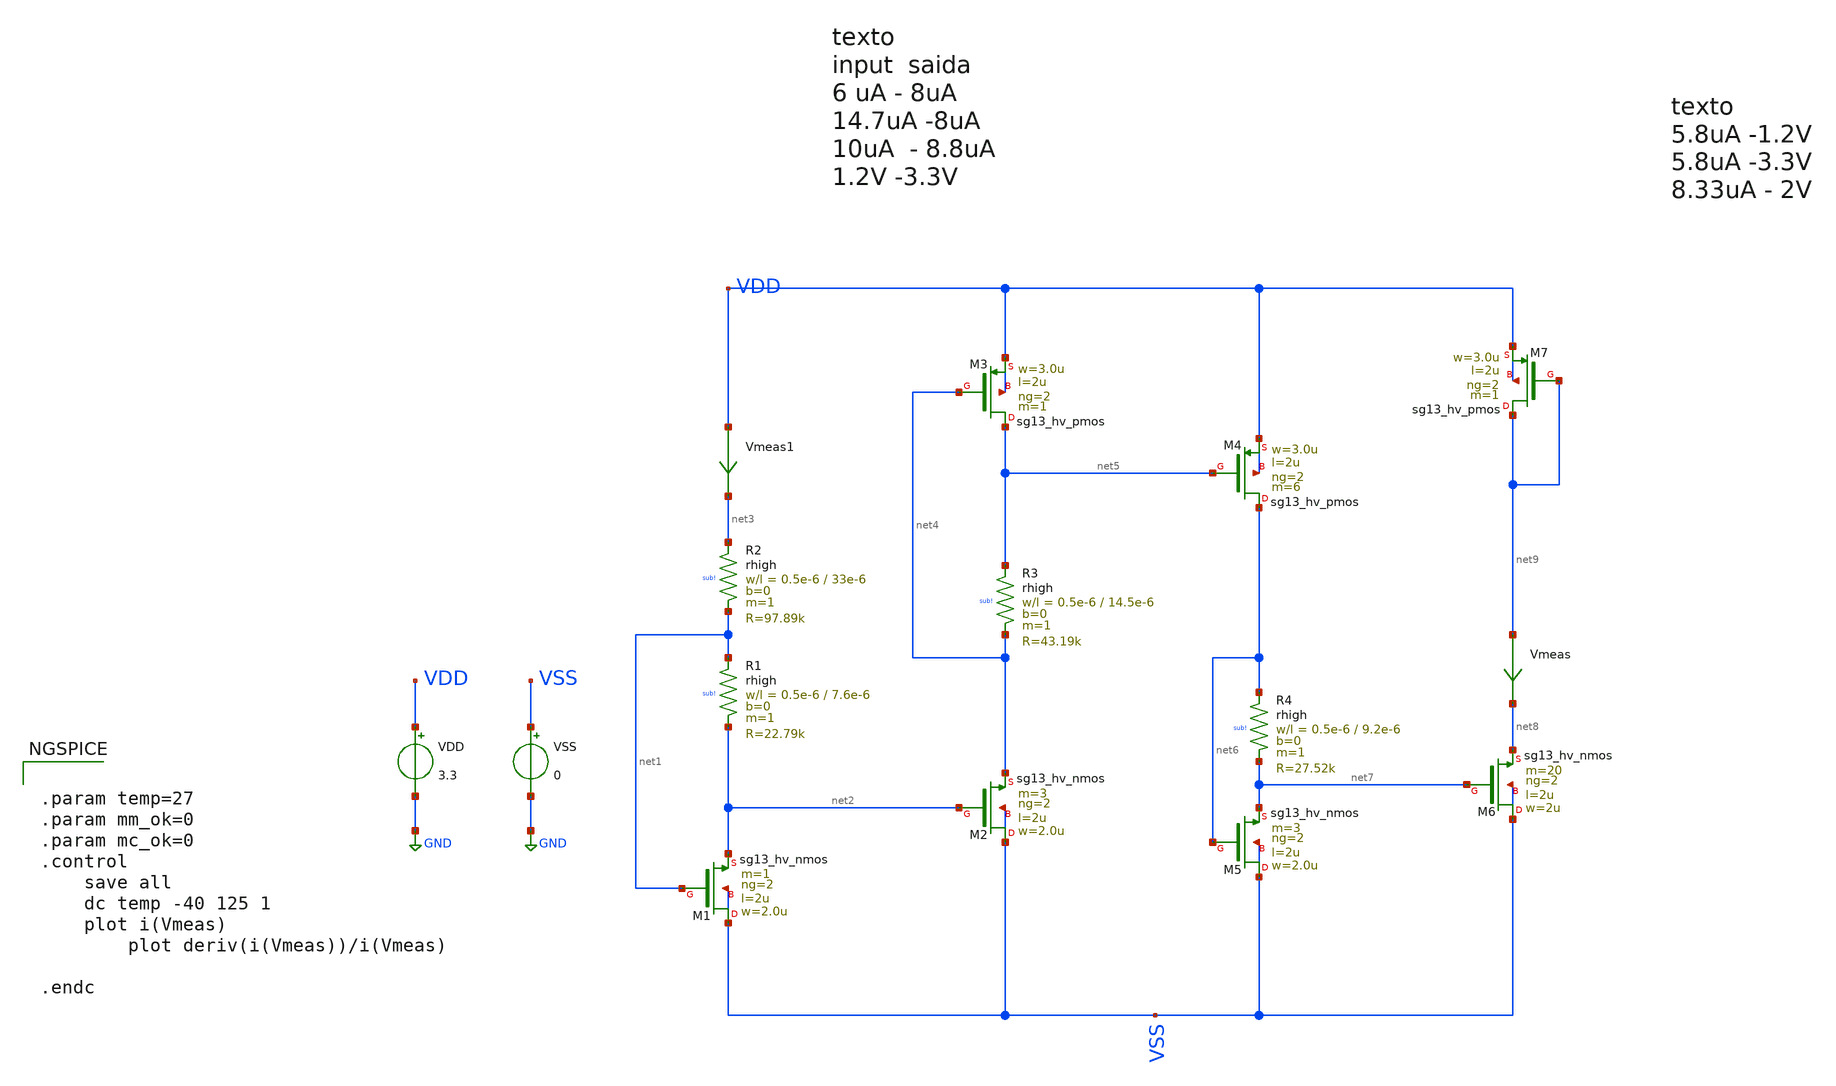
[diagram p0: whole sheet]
** sch_path: Learning/references/CUR_REF_IHP130_3_3/testbench.sch
**.subckt testbench
VDD VDD GND 3.3
VSS VSS GND 0
XR1 net1 net2 sub! rhigh w=0.5e-6 l=7.6e-6 m=1 b=0 mm_ok=1
XM1 VSS net1 net2 VSS sg13_hv_nmos w=2.0u l=2u ng=2 m=1 mm_ok=1
XM2 VSS net2 net4 VSS sg13_hv_nmos w=2.0u l=2u ng=2 m=3 mm_ok=1
XR2 net3 net1 sub! rhigh w=0.5e-6 l=33e-6 m=1 b=0 mm_ok=1
Vmeas1 VDD net3 0
.save i(vmeas1)
XR3 net5 net4 sub! rhigh w=0.5e-6 l=14.5e-6 m=1 b=0 mm_ok=1
XM3 net5 net4 VDD VDD sg13_hv_pmos w=3.0u l=2u ng=2 m=1 mm_ok=1
XM4 net6 net5 VDD VDD sg13_hv_pmos w=3.0u l=2u ng=2 m=6 mm_ok=1
XM5 VSS net6 net7 VSS sg13_hv_nmos w=2.0u l=2u ng=2 m=3 mm_ok=1
XR4 net6 net7 sub! rhigh w=0.5e-6 l=9.2e-6 m=1 b=0 mm_ok=1
Vmeas net9 net8 0
.save i(vmeas)
XM7 net9 net9 VDD VDD sg13_hv_pmos w=3.0u l=2u ng=2 m=1 mm_ok=1
XM6 VSS net7 net8 VSS sg13_hv_nmos w=2u l=2u ng=2 m=20 mm_ok=1
**** begin user architecture code

.lib cornerMOShv.lib mos_tt


.lib $::SG13G2_MODELS/cornerRES.lib res_typ_stat



.param temp=27
.param mm_ok=0
.param mc_ok=0
.control
	save all
	dc temp -40 125 1
	plot i(Vmeas)
        plot deriv(i(Vmeas))/i(Vmeas)

.endc


**** end user architecture code
**.ends
.GLOBAL GND
.end
